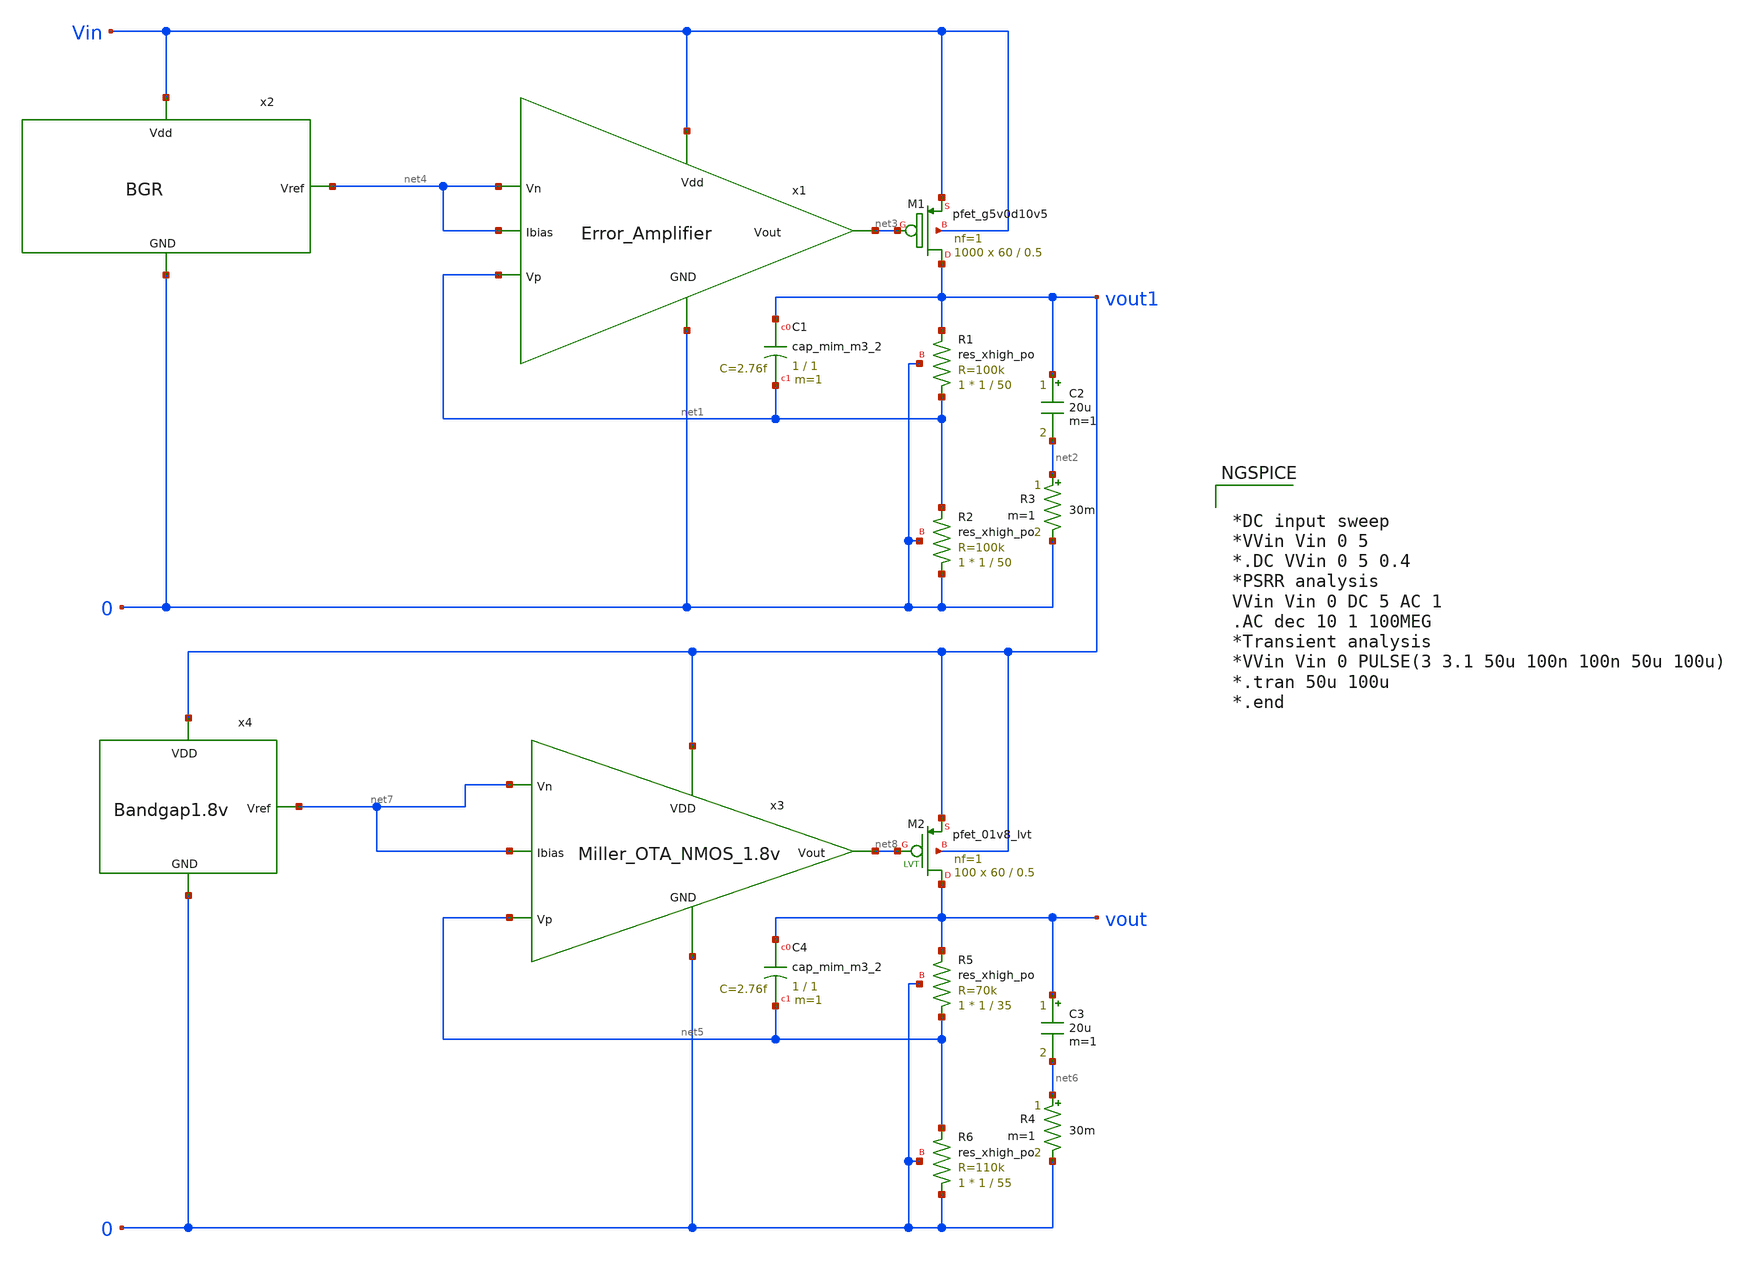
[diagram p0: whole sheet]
** sch_path: LDO/Schematic/LDO.sch
**.subckt LDO
C2 vout1 net2 20u m=1
R3 net2 0 30m m=1
XR1 net1 vout1 0 sky130_fd_pr__res_xhigh_po W=1 L=50 mult=1 m=1
XR2 0 net1 0 sky130_fd_pr__res_xhigh_po W=1 L=50 mult=1 m=1
XC1 vout1 net1 sky130_fd_pr__cap_mim_m3_2 W=1 L=1 MF=1 m=1
XM1 vout1 net3 Vin Vin sky130_fd_pr__pfet_g5v0d10v5 L=0.5 W=60 nf=1 ad='int((nf+1)/2) * W/nf * 0.29'
+ as='int((nf+2)/2) * W/nf * 0.29' pd='2*int((nf+1)/2) * (W/nf + 0.29)' ps='2*int((nf+2)/2) * (W/nf + 0.29)'
+ nrd='0.29 / W' nrs='0.29 / W' sa=0 sb=0 sd=0 mult=1000 m=1000
x1 Vin net4 net1 net3 net4 0 Error_Amplifier
x2 net4 Vin 0 BGR
C3 vout net6 20u m=1
R4 net6 0 30m m=1
XR5 net5 vout 0 sky130_fd_pr__res_xhigh_po W=1 L=35 mult=1 m=1
XR6 0 net5 0 sky130_fd_pr__res_xhigh_po W=1 L=55 mult=1 m=1
XC4 vout net5 sky130_fd_pr__cap_mim_m3_2 W=1 L=1 MF=1 m=1
XM2 vout net8 vout1 vout1 sky130_fd_pr__pfet_01v8_lvt L=0.5 W=60 nf=1 ad='int((nf+1)/2) * W/nf * 0.29'
+ as='int((nf+2)/2) * W/nf * 0.29' pd='2*int((nf+1)/2) * (W/nf + 0.29)' ps='2*int((nf+2)/2) * (W/nf + 0.29)'
+ nrd='0.29 / W' nrs='0.29 / W' sa=0 sb=0 sd=0 mult=100 m=100
x3 vout1 net7 net5 net8 net7 0 Miller_OTA_NMOS_1.8v
x4 net7 vout1 0 Bandgap1.8v
**** begin user architecture code


*DC input sweep
*VVin Vin 0 5
*.DC VVin 0 5 0.4
*PSRR analysis
VVin Vin 0 DC 5 AC 1
.AC dec 10 1 100MEG
*Transient analysis
*VVin Vin 0 PULSE(3 3.1 50u 100n 100n 50u 100u)
*.tran 50u 100u
*.end



.include $::SKYWATER_MODELS/cells/nfet_01v8/sky130_fd_pr__nfet_01v8__tt.corner.spice
.include $::SKYWATER_MODELS/cells/nfet_01v8_lvt/sky130_fd_pr__nfet_01v8_lvt__tt.corner.spice
.include $::SKYWATER_MODELS/cells/pfet_01v8/sky130_fd_pr__pfet_01v8__tt.corner.spice
.include $::SKYWATER_MODELS/cells/nfet_03v3_nvt/sky130_fd_pr__nfet_03v3_nvt__tt.corner.spice
.include $::SKYWATER_MODELS/cells/nfet_05v0_nvt/sky130_fd_pr__nfet_05v0_nvt__tt.corner.spice
.include $::SKYWATER_MODELS/cells/esd_nfet_01v8/sky130_fd_pr__esd_nfet_01v8__tt.corner.spice
.include $::SKYWATER_MODELS/cells/pfet_01v8_lvt/sky130_fd_pr__pfet_01v8_lvt__tt.corner.spice
.include $::SKYWATER_MODELS/cells/pfet_01v8_hvt/sky130_fd_pr__pfet_01v8_hvt__tt.corner.spice
.include $::SKYWATER_MODELS/cells/esd_pfet_g5v0d10v5/sky130_fd_pr__esd_pfet_g5v0d10v5__tt.corner.spice
.include $::SKYWATER_MODELS/cells/pfet_g5v0d10v5/sky130_fd_pr__pfet_g5v0d10v5__tt.corner.spice
.include $::SKYWATER_MODELS/cells/pfet_g5v0d16v0/sky130_fd_pr__pfet_g5v0d16v0__tt.corner.spice
.include $::SKYWATER_MODELS/cells/nfet_g5v0d10v5/sky130_fd_pr__nfet_g5v0d10v5__tt.corner.spice
.include $::SKYWATER_MODELS/cells/nfet_g5v0d16v0/sky130_fd_pr__nfet_g5v0d16v0__tt_discrete.corner.spice
.include $::SKYWATER_MODELS/cells/esd_nfet_g5v0d10v5/sky130_fd_pr__esd_nfet_g5v0d10v5__tt.corner.spice
.include $::SKYWATER_MODELS/models/corners/tt/nonfet.spice
* Mismatch parameters
.include $::SKYWATER_MODELS/cells/nfet_01v8/sky130_fd_pr__nfet_01v8__mismatch.corner.spice
.include $::SKYWATER_MODELS/cells/pfet_01v8/sky130_fd_pr__pfet_01v8__mismatch.corner.spice
.include $::SKYWATER_MODELS/cells/nfet_01v8_lvt/sky130_fd_pr__nfet_01v8_lvt__mismatch.corner.spice
.include $::SKYWATER_MODELS/cells/pfet_01v8_lvt/sky130_fd_pr__pfet_01v8_lvt__mismatch.corner.spice
.include $::SKYWATER_MODELS/cells/pfet_01v8_hvt/sky130_fd_pr__pfet_01v8_hvt__mismatch.corner.spice
.include $::SKYWATER_MODELS/cells/nfet_g5v0d10v5/sky130_fd_pr__nfet_g5v0d10v5__mismatch.corner.spice
.include $::SKYWATER_MODELS/cells/pfet_g5v0d10v5/sky130_fd_pr__pfet_g5v0d10v5__mismatch.corner.spice
.include $::SKYWATER_MODELS/cells/nfet_05v0_nvt/sky130_fd_pr__nfet_05v0_nvt__mismatch.corner.spice
.include $::SKYWATER_MODELS/cells/nfet_03v3_nvt/sky130_fd_pr__nfet_03v3_nvt__mismatch.corner.spice
* Resistor$::SKYWATER_MODELS/Capacitor
.include $::SKYWATER_MODELS/models/r+c/res_typical__cap_typical.spice
.include $::SKYWATER_MODELS/models/r+c/res_typical__cap_typical__lin.spice
* Special cells
.include $::SKYWATER_MODELS/models/corners/tt/specialized_cells.spice
* All models
.include $::SKYWATER_MODELS/models/all.spice
* Corner
.include $::SKYWATER_MODELS/models/corners/tt/rf.spice

**** end user architecture code
**.ends
.end
